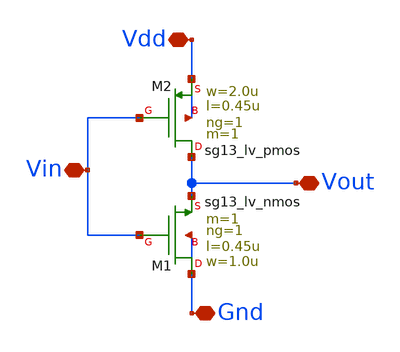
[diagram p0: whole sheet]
** sch_path: conformance/ihp-ngspice-provider-analyses/artifacts/native-replay/generated/inverter-source/inverter.sch
**.subckt inverter Vout Vdd Vin Gnd
*.iopin Vout
*.iopin Vdd
*.iopin Vin
*.iopin Gnd
XM1 Gnd Vin Vout Gnd sg13_lv_nmos w=1.0u l=0.45u ng=1 m=1 mm_ok=1
XM2 Vout Vin Vdd Vdd sg13_lv_pmos w=2.0u l=0.45u ng=1 m=1 mm_ok=1
**.ends
.end
